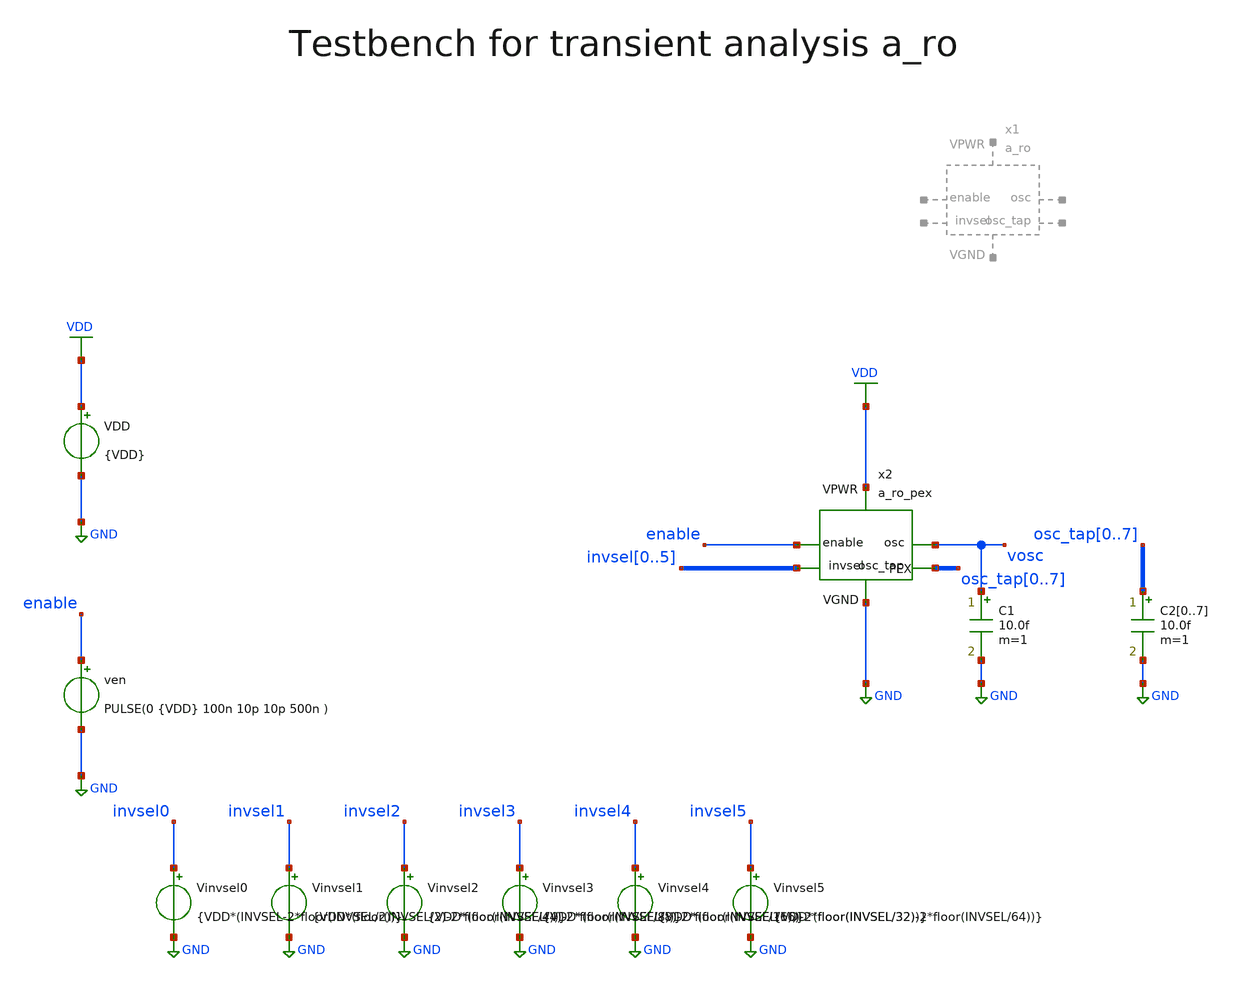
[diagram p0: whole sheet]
** sch_path: macros/heichips26_digital_project/macros/a_ro/testbenches/xschem/a_ro_tb_tran.sch
**.subckt a_ro_tb_tran
VDD VDD GND {VDD}
ven enable GND PULSE(0 {VDD} 100n 10p 10p 500n )
x2 VDD GND enable vosc osc_tap0 osc_tap1 osc_tap2 osc_tap3 osc_tap4 osc_tap5 osc_tap6 osc_tap7
+ invsel0 invsel1 invsel2 invsel3 invsel4 invsel5 a_ro_pex
C1 vosc GND 10.0f m=1
Vinvsel0 invsel0 GND {VDD*(INVSEL-2*floor(INVSEL/2))}
Vinvsel1 invsel1 GND {VDD*(floor(INVSEL/2)-2*floor(INVSEL/4))}
Vinvsel2 invsel2 GND {VDD*(floor(INVSEL/4)-2*floor(INVSEL/8))}
Vinvsel3 invsel3 GND {VDD*(floor(INVSEL/8)-2*floor(INVSEL/16))}
Vinvsel4 invsel4 GND {VDD*(floor(INVSEL/16)-2*floor(INVSEL/32))}
Vinvsel5 invsel5 GND {VDD*(floor(INVSEL/32)-2*floor(INVSEL/64))}
C20 osc_tap0 GND 10.0f m=1
C21 osc_tap1 GND 10.0f m=1
C22 osc_tap2 GND 10.0f m=1
C23 osc_tap3 GND 10.0f m=1
C24 osc_tap4 GND 10.0f m=1
C25 osc_tap5 GND 10.0f m=1
C26 osc_tap6 GND 10.0f m=1
C27 osc_tap7 GND 10.0f m=1
**** begin user architecture code


.include ../../../netlist/xspice/a_ro.xspice
.include ../../../netlist/pex/a_ro_magic_pex_3.spice
.param VDD=1.2
* Setting under test: tap select 0..63 (loop = 3 + 16*INVSEL inverters)
.param INVSEL=63
.param temp=27
.options klu method=gear reltol=1e-4 abstol=1e-12 gmin=1e-15
.control

set num_threads=8

*save all

* User Constants
let tstop = 500n
let tstep = 1500p

* Operating Point Analysis
*op
*remzerovec
*write @schname\.raw
*set appendwrite

* Transient Analysis
* 'uic' is needed (the PEX operating point does not converge). The chain starts unsettled, so
* enable stays low for 100 ns (> 1011 stages * t_inv); otherwise several edges circulate after
*+ enable.
save v(enable) v(vosc) v(osc_tap0) v(osc_tap1) v(osc_tap2) v(osc_tap3) v(osc_tap4) v(osc_tap5)
+ v(osc_tap6) v(osc_tap7)
tran $&tstep $&tstop 1n uic
write @schname\.raw

plot v(enable) v(vosc)

* Skip the first edge after enable; two consecutive periods must match (single edge in the loop)
meas tran t_rise1 when v(vosc)=0.6 rise=2
meas tran t_rise2 when v(vosc)=0.6 rise=3
meas tran t_rise3 when v(vosc)=0.6 rise=4
let T_osc = t_rise2 - t_rise1
let T_osc2 = t_rise3 - t_rise2
let f_osc = 1/T_osc
print T_osc T_osc2
print f_osc

* Intermediate taps: every tap must toggle at the RO frequency (check for invsel=0 and invsel=63).
* td=100n: count only edges after enable, the taps also toggle while the chain settles.
meas tran t_tap0_r2 when v(osc_tap0)=0.6 rise=2 td=100n
meas tran t_tap0_r3 when v(osc_tap0)=0.6 rise=3 td=100n
let f_tap0 = 1/(t_tap0_r3 - t_tap0_r2)
meas tran t_tap1_r2 when v(osc_tap1)=0.6 rise=2 td=100n
meas tran t_tap1_r3 when v(osc_tap1)=0.6 rise=3 td=100n
let f_tap1 = 1/(t_tap1_r3 - t_tap1_r2)
meas tran t_tap2_r2 when v(osc_tap2)=0.6 rise=2 td=100n
meas tran t_tap2_r3 when v(osc_tap2)=0.6 rise=3 td=100n
let f_tap2 = 1/(t_tap2_r3 - t_tap2_r2)
meas tran t_tap3_r2 when v(osc_tap3)=0.6 rise=2 td=100n
meas tran t_tap3_r3 when v(osc_tap3)=0.6 rise=3 td=100n
let f_tap3 = 1/(t_tap3_r3 - t_tap3_r2)
meas tran t_tap4_r2 when v(osc_tap4)=0.6 rise=2 td=100n
meas tran t_tap4_r3 when v(osc_tap4)=0.6 rise=3 td=100n
let f_tap4 = 1/(t_tap4_r3 - t_tap4_r2)
meas tran t_tap5_r2 when v(osc_tap5)=0.6 rise=2 td=100n
meas tran t_tap5_r3 when v(osc_tap5)=0.6 rise=3 td=100n
let f_tap5 = 1/(t_tap5_r3 - t_tap5_r2)
meas tran t_tap6_r2 when v(osc_tap6)=0.6 rise=2 td=100n
meas tran t_tap6_r3 when v(osc_tap6)=0.6 rise=3 td=100n
let f_tap6 = 1/(t_tap6_r3 - t_tap6_r2)
meas tran t_tap7_r2 when v(osc_tap7)=0.6 rise=2 td=100n
meas tran t_tap7_r3 when v(osc_tap7)=0.6 rise=3 td=100n
let f_tap7 = 1/(t_tap7_r3 - t_tap7_r2)
print f_tap0 f_tap1 f_tap2 f_tap3 f_tap4 f_tap5 f_tap6 f_tap7

* Writing Data
unset appendwrite
set wr_vecnames
set wr_singlescale
wrdata ../plot_simulations/data/@schname\.txt enable vosc osc_tap0 osc_tap1 osc_tap2 osc_tap3
+ osc_tap4 osc_tap5 osc_tap6 osc_tap7
*quit
.endc


.lib cornerMOSlv.lib mos_tt
.lib cornerMOShv.lib mos_tt
.lib cornerRES.lib res_typ
.lib cornerDIO.lib dio_tt

**** end user architecture code
**.ends
.GLOBAL GND
.GLOBAL VDD
.end
